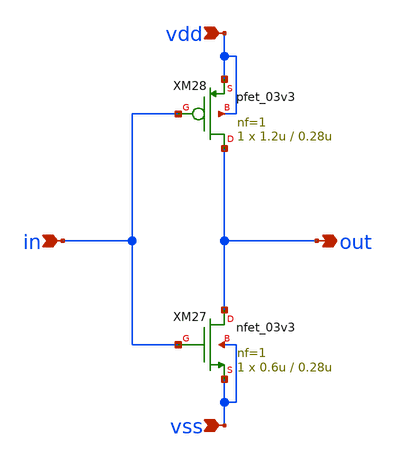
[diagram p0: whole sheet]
** sch_path: xschem/inv.sch
**.subckt inv in vdd vss out
*.ipin in
*.ipin vdd
*.ipin vss
*.opin out
XM27 out in vss vss nfet_03v3 L=0.28u W=0.6u nf=1 ad='int((nf+1)/2) * W/nf * 0.18u' as='int((nf+2)/2) * W/nf * 0.18u'
+ pd='2*int((nf+1)/2) * (W/nf + 0.18u)' ps='2*int((nf+2)/2) * (W/nf + 0.18u)' nrd='0.18u / W' nrs='0.18u / W'
+ sa=0 sb=0 sd=0 m=1
XM28 out in vdd vdd pfet_03v3 L=0.28u W=1.2u nf=1 ad='int((nf+1)/2) * W/nf * 0.18u' as='int((nf+2)/2) * W/nf * 0.18u'
+ pd='2*int((nf+1)/2) * (W/nf + 0.18u)' ps='2*int((nf+2)/2) * (W/nf + 0.18u)' nrd='0.18u / W' nrs='0.18u / W'
+ sa=0 sb=0 sd=0 m=1
**.ends
.end
